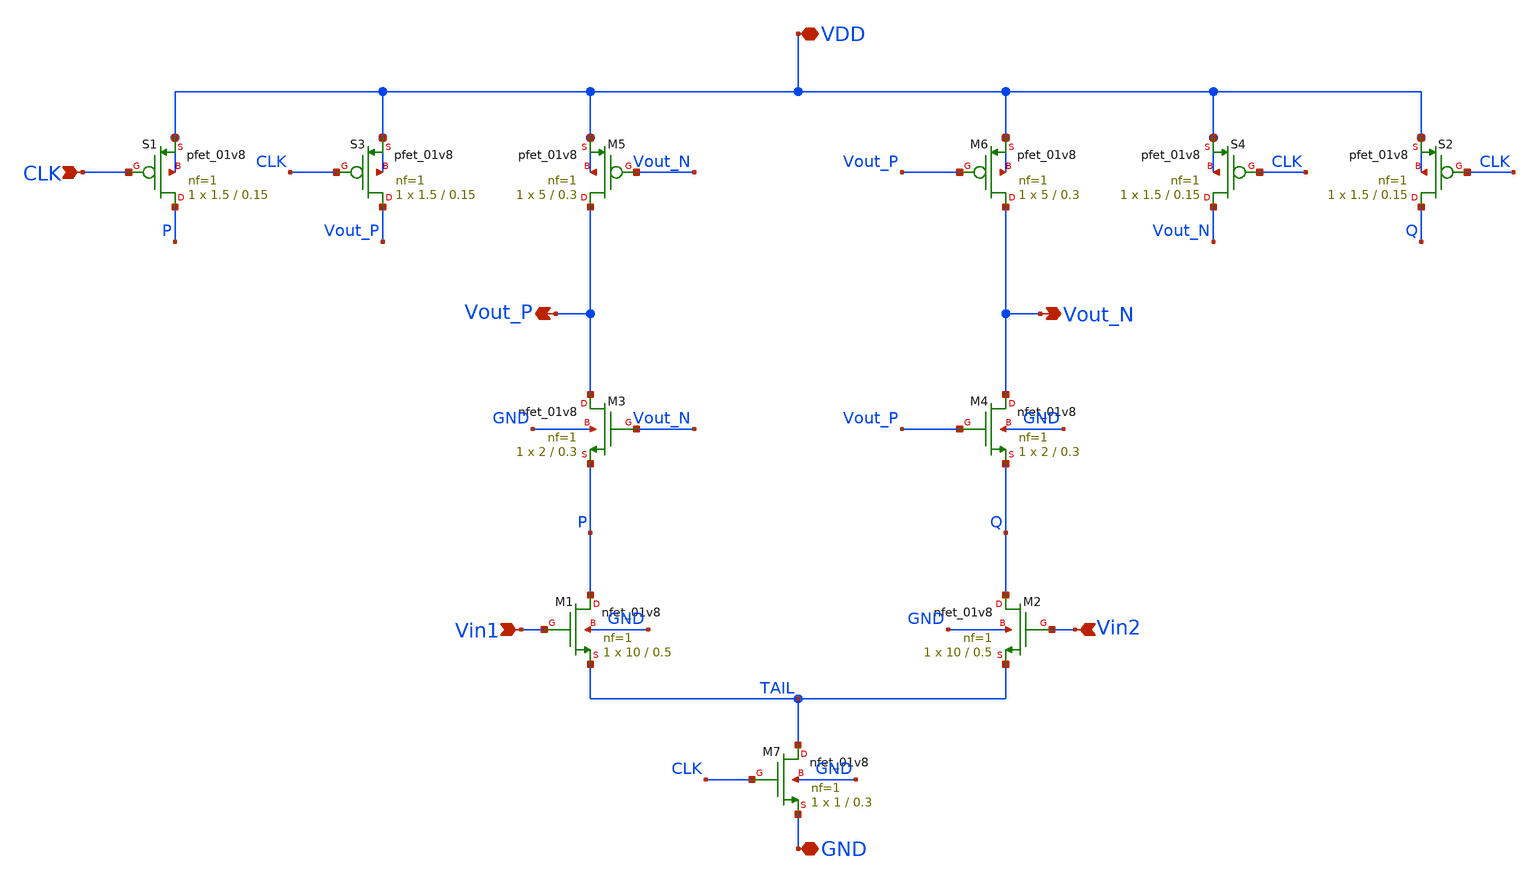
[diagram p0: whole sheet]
** sch_path: blocks/03_StrongARM/xschem/StrongARM.sch
**.subckt StrongARM VDD GND Vin1 Vin2 CLK Vout_P Vout_N
*.iopin VDD
*.iopin GND
*.ipin Vin1
*.ipin Vin2
*.ipin CLK
*.opin Vout_P
*.opin Vout_N
XS1 P CLK VDD VDD sky130_fd_pr__pfet_01v8 L=0.15 W=1.5 nf=1 ad='int((1 + 1)/2) * 1.5 / 1 * 0.29' as='int((1 + 2)/2) * 1.5 / 1 * 0.29'
+ pd='2*int((1 + 1)/2) * (1.5 / 1 + 0.29)' ps='2*int((1 + 2)/2) * (1.5 / 1 + 0.29)' nrd='0.29 / 1.5 ' nrs='0.29 / 1.5 '
+ sa=0 sb=0 sd=0 mult=1 m=1
XS3 Vout_P CLK VDD VDD sky130_fd_pr__pfet_01v8 L=0.15 W=1.5 nf=1 ad='int((1 + 1)/2) * 1.5 / 1 * 0.29'
+ as='int((1 + 2)/2) * 1.5 / 1 * 0.29' pd='2*int((1 + 1)/2) * (1.5 / 1 + 0.29)' ps='2*int((1 + 2)/2) * (1.5 / 1 + 0.29)'
+ nrd='0.29 / 1.5 ' nrs='0.29 / 1.5 ' sa=0 sb=0 sd=0 mult=1 m=1
XM5 Vout_P Vout_N VDD VDD sky130_fd_pr__pfet_01v8 L=0.3 W=5 nf=1 ad='int((1 + 1)/2) * 5 / 1 * 0.29' as='int((1 + 2)/2) * 5 / 1 * 0.29'
+ pd='2*int((1 + 1)/2) * (5 / 1 + 0.29)' ps='2*int((1 + 2)/2) * (5 / 1 + 0.29)' nrd='0.29 / 5 ' nrs='0.29 / 5 '
+ sa=0 sb=0 sd=0 mult=1 m=1
XM6 Vout_N Vout_P VDD VDD sky130_fd_pr__pfet_01v8 L=0.3 W=5 nf=1 ad='int((1 + 1)/2) * 5 / 1 * 0.29' as='int((1 + 2)/2) * 5 / 1 * 0.29'
+ pd='2*int((1 + 1)/2) * (5 / 1 + 0.29)' ps='2*int((1 + 2)/2) * (5 / 1 + 0.29)' nrd='0.29 / 5 ' nrs='0.29 / 5 '
+ sa=0 sb=0 sd=0 mult=1 m=1
XS4 Vout_N CLK VDD VDD sky130_fd_pr__pfet_01v8 L=0.15 W=1.5 nf=1 ad='int((1 + 1)/2) * 1.5 / 1 * 0.29'
+ as='int((1 + 2)/2) * 1.5 / 1 * 0.29' pd='2*int((1 + 1)/2) * (1.5 / 1 + 0.29)' ps='2*int((1 + 2)/2) * (1.5 / 1 + 0.29)'
+ nrd='0.29 / 1.5 ' nrs='0.29 / 1.5 ' sa=0 sb=0 sd=0 mult=1 m=1
XS2 Q CLK VDD VDD sky130_fd_pr__pfet_01v8 L=0.15 W=1.5 nf=1 ad='int((1 + 1)/2) * 1.5 / 1 * 0.29' as='int((1 + 2)/2) * 1.5 / 1 * 0.29'
+ pd='2*int((1 + 1)/2) * (1.5 / 1 + 0.29)' ps='2*int((1 + 2)/2) * (1.5 / 1 + 0.29)' nrd='0.29 / 1.5 ' nrs='0.29 / 1.5 '
+ sa=0 sb=0 sd=0 mult=1 m=1
XM3 Vout_P Vout_N P GND sky130_fd_pr__nfet_01v8 L=0.3 W=2 nf=1 ad='int((1 + 1)/2) * 2 / 1 * 0.29' as='int((1 + 2)/2) * 2 / 1 * 0.29'
+ pd='2*int((1 + 1)/2) * (2 / 1 + 0.29)' ps='2*int((1 + 2)/2) * (2 / 1 + 0.29)' nrd='0.29 / 2 ' nrs='0.29 / 2 '
+ sa=0 sb=0 sd=0 mult=1 m=1
XM4 Vout_N Vout_P Q GND sky130_fd_pr__nfet_01v8 L=0.3 W=2 nf=1 ad='int((1 + 1)/2) * 2 / 1 * 0.29' as='int((1 + 2)/2) * 2 / 1 * 0.29'
+ pd='2*int((1 + 1)/2) * (2 / 1 + 0.29)' ps='2*int((1 + 2)/2) * (2 / 1 + 0.29)' nrd='0.29 / 2 ' nrs='0.29 / 2 '
+ sa=0 sb=0 sd=0 mult=1 m=1
XM1 P Vin1 TAIL GND sky130_fd_pr__nfet_01v8 L=0.5 W=10 nf=1 ad='int((1 + 1)/2) * 10 / 1 * 0.29' as='int((1 + 2)/2) * 10 / 1 * 0.29'
+ pd='2*int((1 + 1)/2) * (10 / 1 + 0.29)' ps='2*int((1 + 2)/2) * (10 / 1 + 0.29)' nrd='0.29 / 10 ' nrs='0.29 / 10 '
+ sa=0 sb=0 sd=0 mult=1 m=1
XM2 Q Vin2 TAIL GND sky130_fd_pr__nfet_01v8 L=0.5 W=10 nf=1 ad='int((1 + 1)/2) * 10 / 1 * 0.29' as='int((1 + 2)/2) * 10 / 1 * 0.29'
+ pd='2*int((1 + 1)/2) * (10 / 1 + 0.29)' ps='2*int((1 + 2)/2) * (10 / 1 + 0.29)' nrd='0.29 / 10 ' nrs='0.29 / 10 '
+ sa=0 sb=0 sd=0 mult=1 m=1
XM7 TAIL CLK GND GND sky130_fd_pr__nfet_01v8 L=0.3 W=1 nf=1 ad='int((1 + 1)/2) * 1 / 1 * 0.29' as='int((1 + 2)/2) * 1 / 1 * 0.29'
+ pd='2*int((1 + 1)/2) * (1 / 1 + 0.29)' ps='2*int((1 + 2)/2) * (1 / 1 + 0.29)' nrd='0.29 / 1 ' nrs='0.29 / 1 '
+ sa=0 sb=0 sd=0 mult=1 m=1
**.ends
.end
